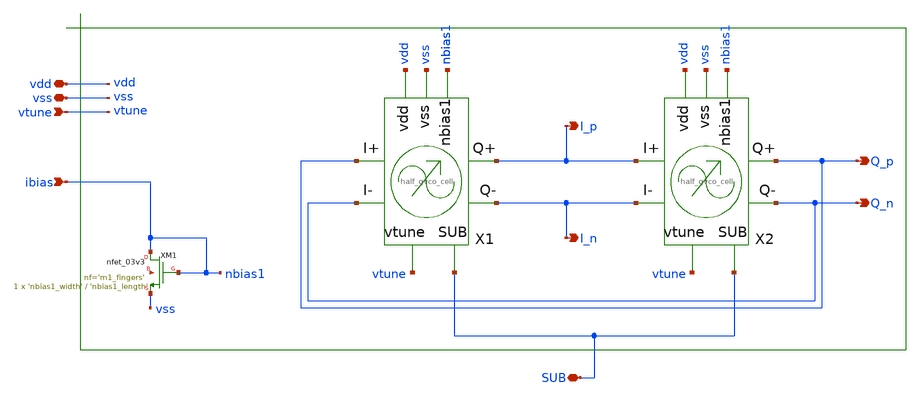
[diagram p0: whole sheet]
** sch_path: sch/vco/vco_quadrature_lc.sch
**.subckt vco_quadrature_lc vdd vss vtune I_p I_n Q_p Q_n ibias SUB
*.iopin vdd
*.iopin vss
*.ipin vtune
*.opin I_p
*.opin I_n
*.opin Q_p
*.opin Q_n
*.ipin ibias
*.iopin SUB
X1 vdd vss nbias1 Q_p Q_n I_p I_n vtune SUB half_qvco_cell m=1
X2 vdd vss nbias1 I_p I_n Q_p Q_n vtune SUB half_qvco_cell m=1
XM1 nbias1 nbias1 vss net1 nfet_03v3 L='nbias1_length' W='nbias1_width' nf='m1_fingers' ad='int((nf+1)/2) * W/nf * 0.18u'
+ as='int((nf+2)/2) * W/nf * 0.18u' pd='2*int((nf+1)/2) * (W/nf + 0.18u)' ps='2*int((nf+2)/2) * (W/nf + 0.18u)'
+ nrd='0.18u / W' nrs='0.18u / W' sa=0 sb=0 sd=0 m=1
**.ends
.end
